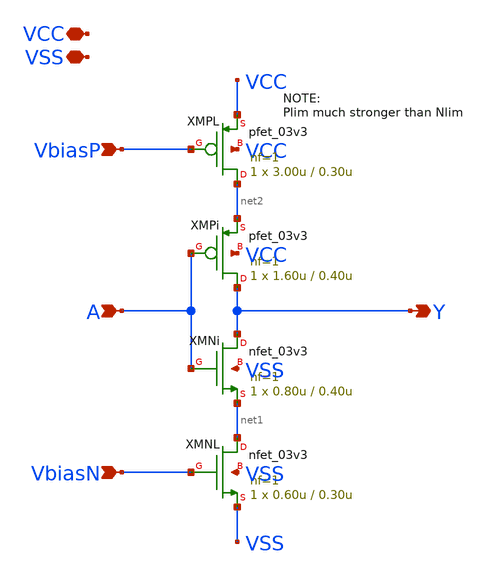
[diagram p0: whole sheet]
** sch_path: xschem/csrostage.sch
**.subckt csrostage VCC VSS A Y VbiasP VbiasN
*.iopin VCC
*.iopin VSS
*.ipin A
*.opin Y
*.ipin VbiasP
*.ipin VbiasN
XMNi Y A net1 VSS nfet_03v3 L=0.40u W=0.80u nf=1 ad='int((nf+1)/2) * W/nf * 0.18u' as='int((nf+2)/2) * W/nf * 0.18u'
+ pd='2*int((nf+1)/2) * (W/nf + 0.18u)' ps='2*int((nf+2)/2) * (W/nf + 0.18u)' nrd='0.18u / W' nrs='0.18u / W'
+ sa=0 sb=0 sd=0 m=1
XMPi Y A net2 VCC pfet_03v3 L=0.40u W=1.60u nf=1 ad='int((nf+1)/2) * W/nf * 0.18u' as='int((nf+2)/2) * W/nf * 0.18u'
+ pd='2*int((nf+1)/2) * (W/nf + 0.18u)' ps='2*int((nf+2)/2) * (W/nf + 0.18u)' nrd='0.18u / W' nrs='0.18u / W'
+ sa=0 sb=0 sd=0 m=1
XMPL net2 VbiasP VCC VCC pfet_03v3 L=0.30u W=3.00u nf=1 ad='int((nf+1)/2) * W/nf * 0.18u' as='int((nf+2)/2) * W/nf * 0.18u'
+ pd='2*int((nf+1)/2) * (W/nf + 0.18u)' ps='2*int((nf+2)/2) * (W/nf + 0.18u)' nrd='0.18u / W' nrs='0.18u / W'
+ sa=0 sb=0 sd=0 m=1
XMNL net1 VbiasN VSS VSS nfet_03v3 L=0.30u W=0.60u nf=1 ad='int((nf+1)/2) * W/nf * 0.18u' as='int((nf+2)/2) * W/nf * 0.18u'
+ pd='2*int((nf+1)/2) * (W/nf + 0.18u)' ps='2*int((nf+2)/2) * (W/nf + 0.18u)' nrd='0.18u / W' nrs='0.18u / W'
+ sa=0 sb=0 sd=0 m=1
**.ends
.end
